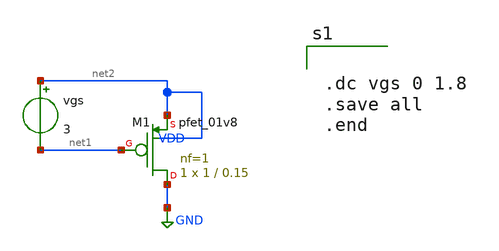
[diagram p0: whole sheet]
** sch_path: xschem/pmos.sch
**.subckt pmos
XM1 GND net1 net2 VDD sky130_fd_pr__pfet_01v8 L=0.15 W=1 nf=1 ad='int((nf+1)/2) * W/nf * 0.29' as='int((nf+2)/2) * W/nf * 0.29'
+ pd='2*int((nf+1)/2) * (W/nf + 0.29)' ps='2*int((nf+2)/2) * (W/nf + 0.29)' nrd='0.29 / W' nrs='0.29 / W'
+ sa=0 sb=0 sd=0 mult=1 m=1
vgs net2 net1 3
**** begin user architecture code


.dc vgs 0 1.8
.save all
.end



** opencircuitdesign pdks install
.lib $::SKYWATER_MODELS/sky130.lib.spice tt


**** end user architecture code
**.ends
.GLOBAL GND
.end
